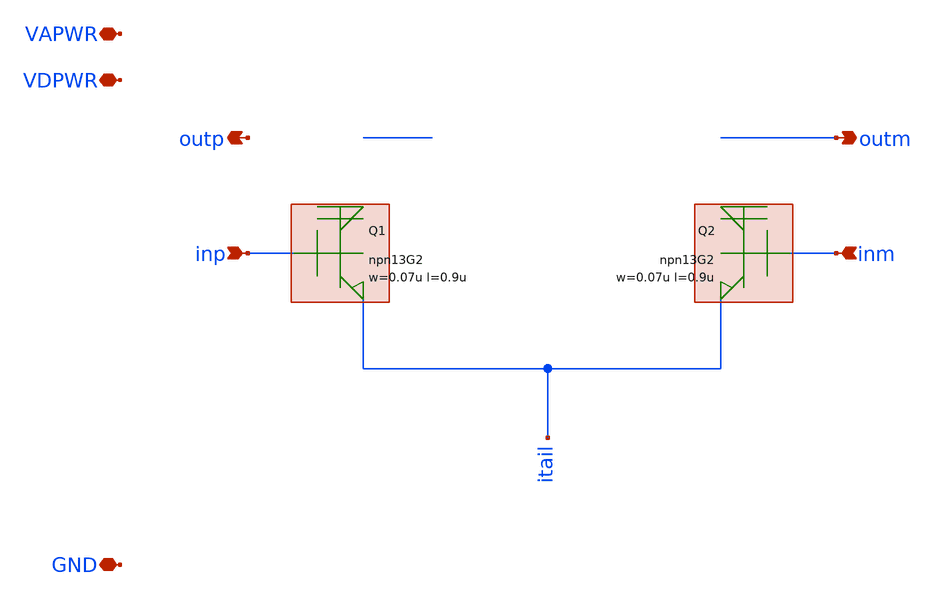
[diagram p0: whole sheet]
** sch_path: xschem/diff_npn.sch
**.subckt diff_npn VAPWR VDPWR GND inp inm outp outm
*.iopin VAPWR
*.iopin VDPWR
*.iopin GND
*.ipin inp
*.ipin inm
*.opin outp
*.opin outm
KQ1 npn13G2 w=0.07u l=0.9u nx=1 ny=1
KQ2 npn13G2 w=0.07u l=0.9u nx=1 ny=1
**.ends
.end
